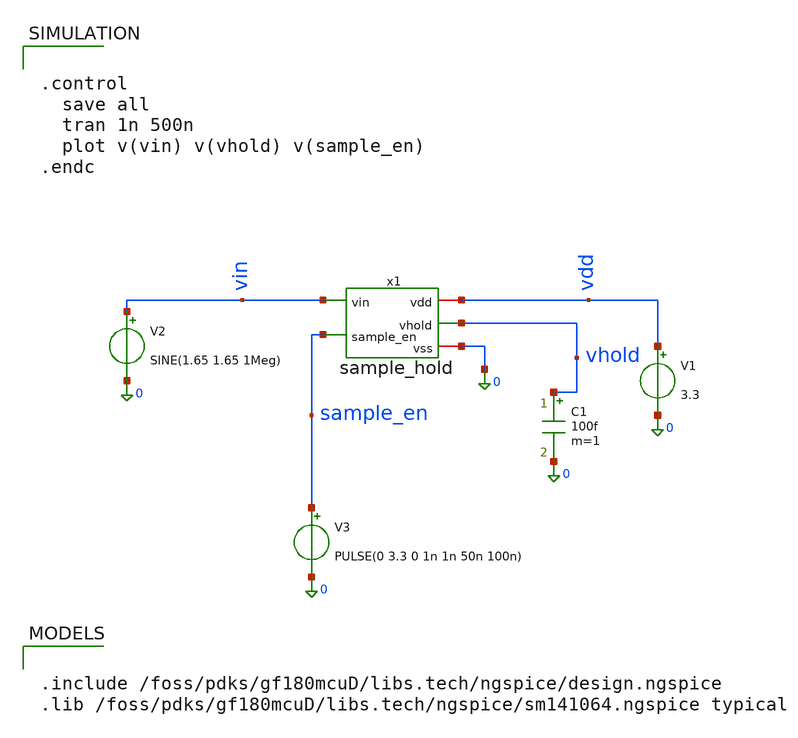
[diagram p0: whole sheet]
** sch_path: xschem/sar_adc/blocks/sample_hold/testbench/tb_sample_hold.sch
**.subckt tb_sample_hold
V1 vdd 0 3.3
V2 vin 0 SINE(1.65 1.65 1Meg)
V3 sample_en 0 PULSE(0 3.3 0 1n 1n 50n 100n)
C1 vhold 0 100f m=1
x1 vin sample_en vhold vdd 0 sample_hold
**** begin user architecture code


.include /foss/pdks/gf180mcuD/libs.tech/ngspice/design.ngspice
.lib /foss/pdks/gf180mcuD/libs.tech/ngspice/sm141064.ngspice typical




.control
  save all
  tran 1n 500n
  plot v(vin) v(vhold) v(sample_en)
.endc


**** end user architecture code
**.ends

* expanding   symbol:  sar_adc/blocks/sample_hold/sample_hold.sym # of pins=5
** sym_path: xschem/sar_adc/blocks/sample_hold/sample_hold.sym
** sch_path: xschem/sar_adc/blocks/sample_hold/sample_hold.sch
.subckt sample_hold vin sample_en vhold vdd vss
*.ipin vin
*.ipin sample_en
*.opin vhold
*.iopin vdd
*.iopin vss
C1 net1 vg 500f m=1
C2 vhold vss 200f m=1
XM1 vin vg vhold vss nfet_03v3 L=0.28u W=5u nf=1 ad='int((nf+1)/2) * W/nf * 0.18u' as='int((nf+2)/2) * W/nf * 0.18u'
+ pd='2*int((nf+1)/2) * (W/nf + 0.18u)' ps='2*int((nf+2)/2) * (W/nf + 0.18u)' nrd='0.18u / W' nrs='0.18u / W'
+ sa=0 sb=0 sd=0 m=1
XM2 vin clkb vhold vdd pfet_03v3 L=0.28u W=5u nf=1 ad='int((nf+1)/2) * W/nf * 0.18u' as='int((nf+2)/2) * W/nf * 0.18u'
+ pd='2*int((nf+1)/2) * (W/nf + 0.18u)' ps='2*int((nf+2)/2) * (W/nf + 0.18u)' nrd='0.18u / W' nrs='0.18u / W'
+ sa=0 sb=0 sd=0 m=1
XM3 net1 clkb vss vss nfet_03v3 L=0.28u W=2u nf=1 ad='int((nf+1)/2) * W/nf * 0.18u' as='int((nf+2)/2) * W/nf * 0.18u'
+ pd='2*int((nf+1)/2) * (W/nf + 0.18u)' ps='2*int((nf+2)/2) * (W/nf + 0.18u)' nrd='0.18u / W' nrs='0.18u / W'
+ sa=0 sb=0 sd=0 m=1
XM4 net1 sample_en vin vss nfet_03v3 L=0.28u W=2u nf=1 ad='int((nf+1)/2) * W/nf * 0.18u' as='int((nf+2)/2) * W/nf * 0.18u'
+ pd='2*int((nf+1)/2) * (W/nf + 0.18u)' ps='2*int((nf+2)/2) * (W/nf + 0.18u)' nrd='0.18u / W' nrs='0.18u / W'
+ sa=0 sb=0 sd=0 m=1
XM5 vg vg vdd vdd pfet_03v3 L=0.28u W=2u nf=1 ad='int((nf+1)/2) * W/nf * 0.18u' as='int((nf+2)/2) * W/nf * 0.18u'
+ pd='2*int((nf+1)/2) * (W/nf + 0.18u)' ps='2*int((nf+2)/2) * (W/nf + 0.18u)' nrd='0.18u / W' nrs='0.18u / W'
+ sa=0 sb=0 sd=0 m=1
XM6 vg clkb vg vdd pfet_03v3 L=0.28u W=2u nf=1 ad='int((nf+1)/2) * W/nf * 0.18u' as='int((nf+2)/2) * W/nf * 0.18u'
+ pd='2*int((nf+1)/2) * (W/nf + 0.18u)' ps='2*int((nf+2)/2) * (W/nf + 0.18u)' nrd='0.18u / W' nrs='0.18u / W'
+ sa=0 sb=0 sd=0 m=1
XM7 vg vdd net2 vss nfet_03v3 L=0.28u W=2u nf=1 ad='int((nf+1)/2) * W/nf * 0.18u' as='int((nf+2)/2) * W/nf * 0.18u'
+ pd='2*int((nf+1)/2) * (W/nf + 0.18u)' ps='2*int((nf+2)/2) * (W/nf + 0.18u)' nrd='0.18u / W' nrs='0.18u / W'
+ sa=0 sb=0 sd=0 m=1
XM8 net2 clkb vss vss nfet_03v3 L=0.28u W=2u nf=1 ad='int((nf+1)/2) * W/nf * 0.18u' as='int((nf+2)/2) * W/nf * 0.18u'
+ pd='2*int((nf+1)/2) * (W/nf + 0.18u)' ps='2*int((nf+2)/2) * (W/nf + 0.18u)' nrd='0.18u / W' nrs='0.18u / W'
+ sa=0 sb=0 sd=0 m=1
xinv2 vdd clkb sample_en vss inv_sh
.ends


* expanding   symbol:  sar_adc/blocks/sample_hold/inv_sh.sym # of pins=4
** sym_path: xschem/sar_adc/blocks/sample_hold/inv_sh.sym
** sch_path: xschem/sar_adc/blocks/sample_hold/inv_sh.sch
.subckt inv_sh vdd vo vi vss
*.iopin vdd
*.ipin vi
*.opin vo
*.iopin vss
XM1 vo vi vss vss nfet_03v3 L=0.28u W=1u nf=1 ad='int((nf+1)/2) * W/nf * 0.18u' as='int((nf+2)/2) * W/nf * 0.18u'
+ pd='2*int((nf+1)/2) * (W/nf + 0.18u)' ps='2*int((nf+2)/2) * (W/nf + 0.18u)' nrd='0.18u / W' nrs='0.18u / W'
+ sa=0 sb=0 sd=0 m=1
XM2 vo vi vdd vdd pfet_03v3 L=0.28u W=2u nf=1 ad='int((nf+1)/2) * W/nf * 0.18u' as='int((nf+2)/2) * W/nf * 0.18u'
+ pd='2*int((nf+1)/2) * (W/nf + 0.18u)' ps='2*int((nf+2)/2) * (W/nf + 0.18u)' nrd='0.18u / W' nrs='0.18u / W'
+ sa=0 sb=0 sd=0 m=1
.ends

.end
